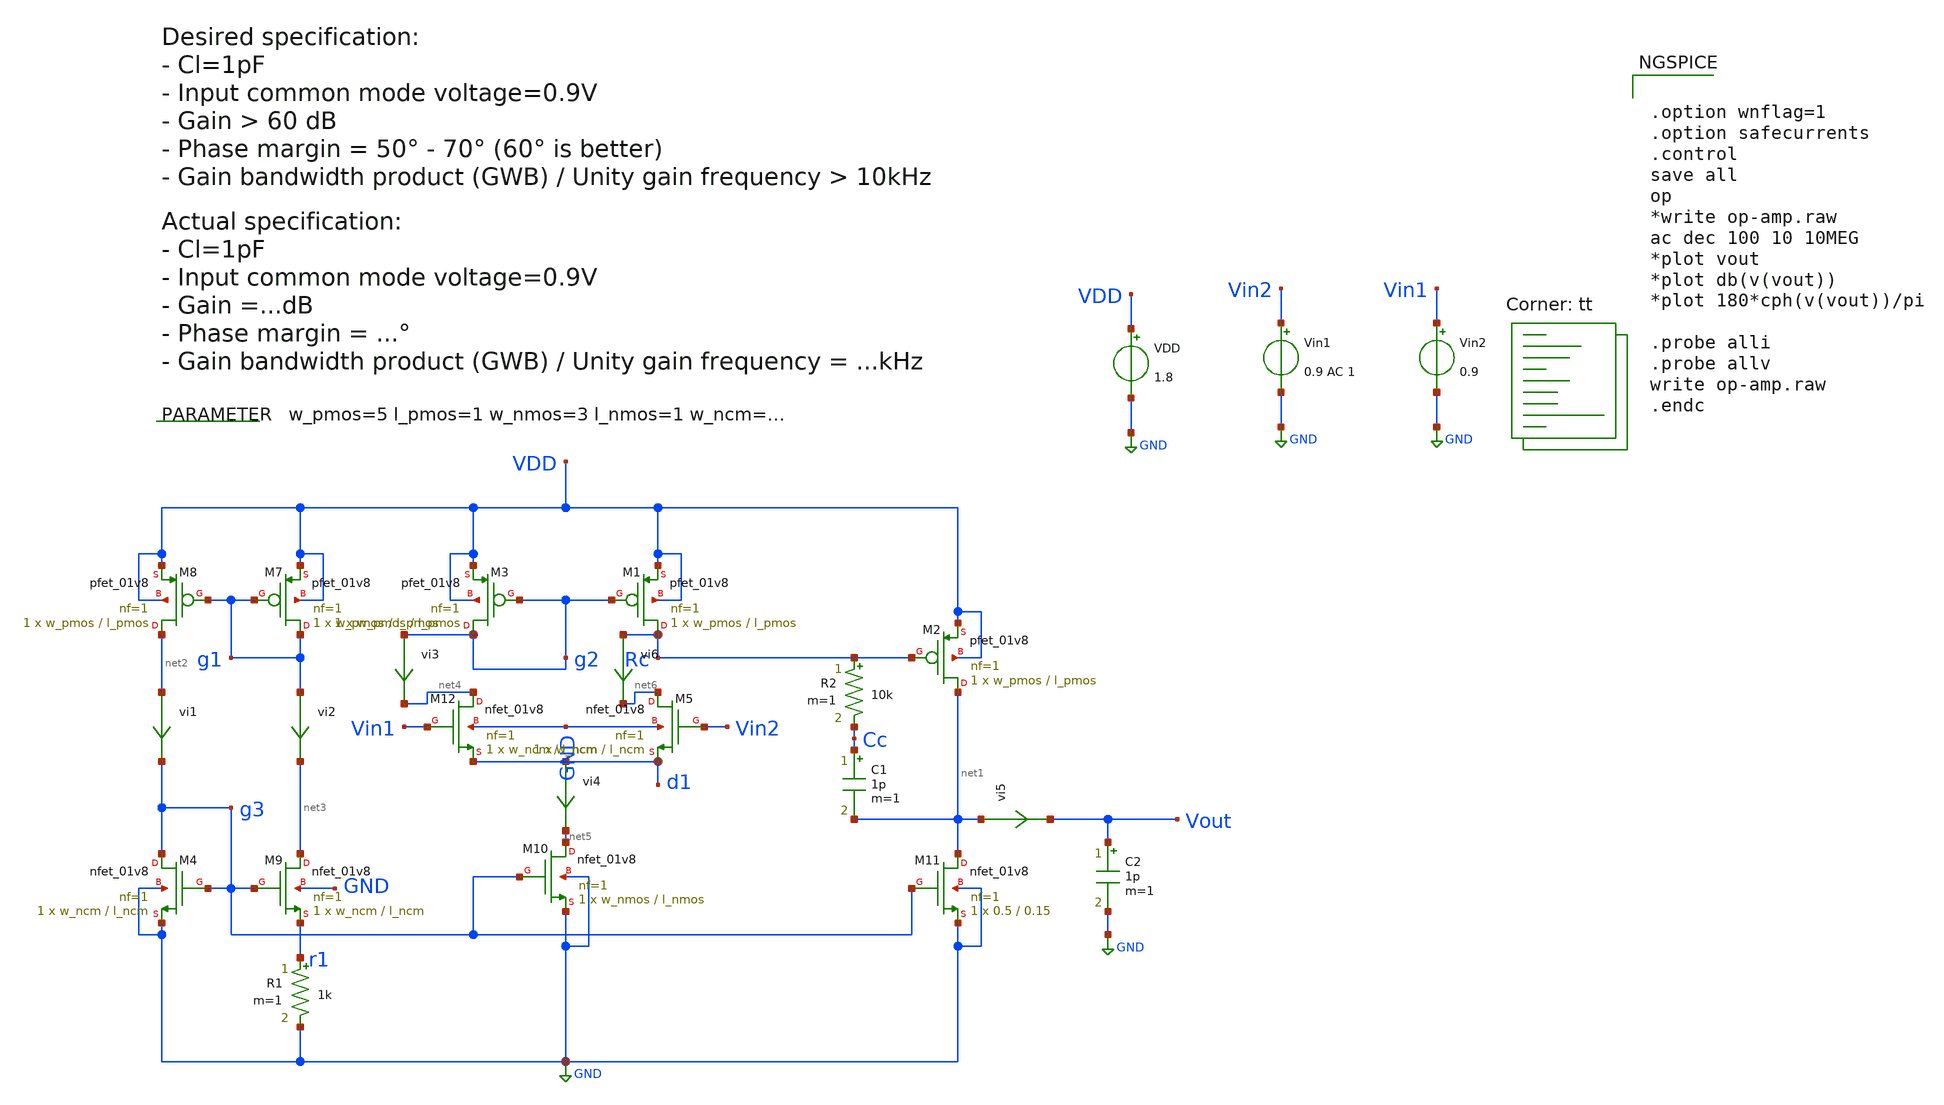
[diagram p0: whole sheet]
** sch_path: xschem/op-amp.sch
**.subckt op-amp
XM3 g2 g2 VDD VDD sky130_fd_pr__pfet_01v8 L=l_pmos W=w_pmos nf=1 ad='int((nf+1)/2) * W/nf * 0.29' as='int((nf+2)/2) * W/nf * 0.29'
+ pd='2*int((nf+1)/2) * (W/nf + 0.29)' ps='2*int((nf+2)/2) * (W/nf + 0.29)' nrd='0.29 / W' nrs='0.29 / W'
+ sa=0 sb=0 sd=0 mult=1 m=1
XM9 net3 g3 r1 GND sky130_fd_pr__nfet_01v8 L=l_ncm W=w_ncm nf=1 ad='int((nf+1)/2) * W/nf * 0.29' as='int((nf+2)/2) * W/nf * 0.29'
+ pd='2*int((nf+1)/2) * (W/nf + 0.29)' ps='2*int((nf+2)/2) * (W/nf + 0.29)' nrd='0.29 / W' nrs='0.29 / W'
+ sa=0 sb=0 sd=0 mult=1 m=1
XM10 net5 g3 GND GND sky130_fd_pr__nfet_01v8 L=l_nmos W=w_nmos nf=1 ad='int((nf+1)/2) * W/nf * 0.29'
+ as='int((nf+2)/2) * W/nf * 0.29' pd='2*int((nf+1)/2) * (W/nf + 0.29)' ps='2*int((nf+2)/2) * (W/nf + 0.29)'
+ nrd='0.29 / W' nrs='0.29 / W' sa=0 sb=0 sd=0 mult=1 m=1
XM11 net1 g3 GND GND sky130_fd_pr__nfet_01v8 L=0.15 W=0.5 nf=1 ad='int((nf+1)/2) * W/nf * 0.29' as='int((nf+2)/2) * W/nf * 0.29'
+ pd='2*int((nf+1)/2) * (W/nf + 0.29)' ps='2*int((nf+2)/2) * (W/nf + 0.29)' nrd='0.29 / W' nrs='0.29 / W'
+ sa=0 sb=0 sd=0 mult=1 m=1
R1 r1 GND 1k m=1
R2 Rc Cc 10k m=1
C1 Cc net1 1p m=1
C2 Vout GND 1p m=1
VDD VDD GND 1.8
Vin1 Vin2 GND 0.9 AC 1
Vin2 Vin1 GND 0.9
vi1 net2 g3 0
.save i(vi1)
vi2 g1 net3 0
.save i(vi2)
vi3 g2 net4 0
.save i(vi3)
vi4 d1 net5 0
.save i(vi4)
vi5 net1 Vout 0
.save i(vi5)
vi6 Rc net6 0
.save i(vi6)
.param w_pmos=5 l_pmos=1 w_nmos=3 l_nmos=1 w_ncm=1.5 l_ncm=1
XM1 Rc g2 VDD VDD sky130_fd_pr__pfet_01v8 L=l_pmos W=w_pmos nf=1 ad='int((nf+1)/2) * W/nf * 0.29' as='int((nf+2)/2) * W/nf * 0.29'
+ pd='2*int((nf+1)/2) * (W/nf + 0.29)' ps='2*int((nf+2)/2) * (W/nf + 0.29)' nrd='0.29 / W' nrs='0.29 / W'
+ sa=0 sb=0 sd=0 mult=1 m=1
XM2 net1 Rc VDD VDD sky130_fd_pr__pfet_01v8 L=l_pmos W=w_pmos nf=1 ad='int((nf+1)/2) * W/nf * 0.29' as='int((nf+2)/2) * W/nf * 0.29'
+ pd='2*int((nf+1)/2) * (W/nf + 0.29)' ps='2*int((nf+2)/2) * (W/nf + 0.29)' nrd='0.29 / W' nrs='0.29 / W'
+ sa=0 sb=0 sd=0 mult=1 m=1
XM7 g1 g1 VDD VDD sky130_fd_pr__pfet_01v8 L=l_pmos W=w_pmos nf=1 ad='int((nf+1)/2) * W/nf * 0.29' as='int((nf+2)/2) * W/nf * 0.29'
+ pd='2*int((nf+1)/2) * (W/nf + 0.29)' ps='2*int((nf+2)/2) * (W/nf + 0.29)' nrd='0.29 / W' nrs='0.29 / W'
+ sa=0 sb=0 sd=0 mult=1 m=1
XM8 net2 g1 VDD VDD sky130_fd_pr__pfet_01v8 L=l_pmos W=w_pmos nf=1 ad='int((nf+1)/2) * W/nf * 0.29' as='int((nf+2)/2) * W/nf * 0.29'
+ pd='2*int((nf+1)/2) * (W/nf + 0.29)' ps='2*int((nf+2)/2) * (W/nf + 0.29)' nrd='0.29 / W' nrs='0.29 / W'
+ sa=0 sb=0 sd=0 mult=1 m=1
XM4 g3 g3 GND GND sky130_fd_pr__nfet_01v8 L=l_ncm W=w_ncm nf=1 ad='int((nf+1)/2) * W/nf * 0.29' as='int((nf+2)/2) * W/nf * 0.29'
+ pd='2*int((nf+1)/2) * (W/nf + 0.29)' ps='2*int((nf+2)/2) * (W/nf + 0.29)' nrd='0.29 / W' nrs='0.29 / W'
+ sa=0 sb=0 sd=0 mult=1 m=1
XM12 net4 Vin1 d1 GND sky130_fd_pr__nfet_01v8 L=l_ncm W=w_ncm nf=1 ad='int((nf+1)/2) * W/nf * 0.29' as='int((nf+2)/2) * W/nf * 0.29'
+ pd='2*int((nf+1)/2) * (W/nf + 0.29)' ps='2*int((nf+2)/2) * (W/nf + 0.29)' nrd='0.29 / W' nrs='0.29 / W'
+ sa=0 sb=0 sd=0 mult=1 m=1
XM5 net6 Vin2 d1 GND sky130_fd_pr__nfet_01v8 L=l_ncm W=w_ncm nf=1 ad='int((nf+1)/2) * W/nf * 0.29' as='int((nf+2)/2) * W/nf * 0.29'
+ pd='2*int((nf+1)/2) * (W/nf + 0.29)' ps='2*int((nf+2)/2) * (W/nf + 0.29)' nrd='0.29 / W' nrs='0.29 / W'
+ sa=0 sb=0 sd=0 mult=1 m=1
**** begin user architecture code
 .lib $::SKYWATER_MODELS/sky130.lib.spice tt

.param mc_mm_switch = 0
.param mc_pr_switch = 0



.option wnflag=1
.option safecurrents
.control
save all
op
*write op-amp.raw
ac dec 100 10 10MEG
*plot vout
*plot db(v(vout))
*plot 180*cph(v(vout))/pi

.probe alli
.probe allv
write op-amp.raw
.endc


**** end user architecture code
**.ends
.GLOBAL GND
.end
